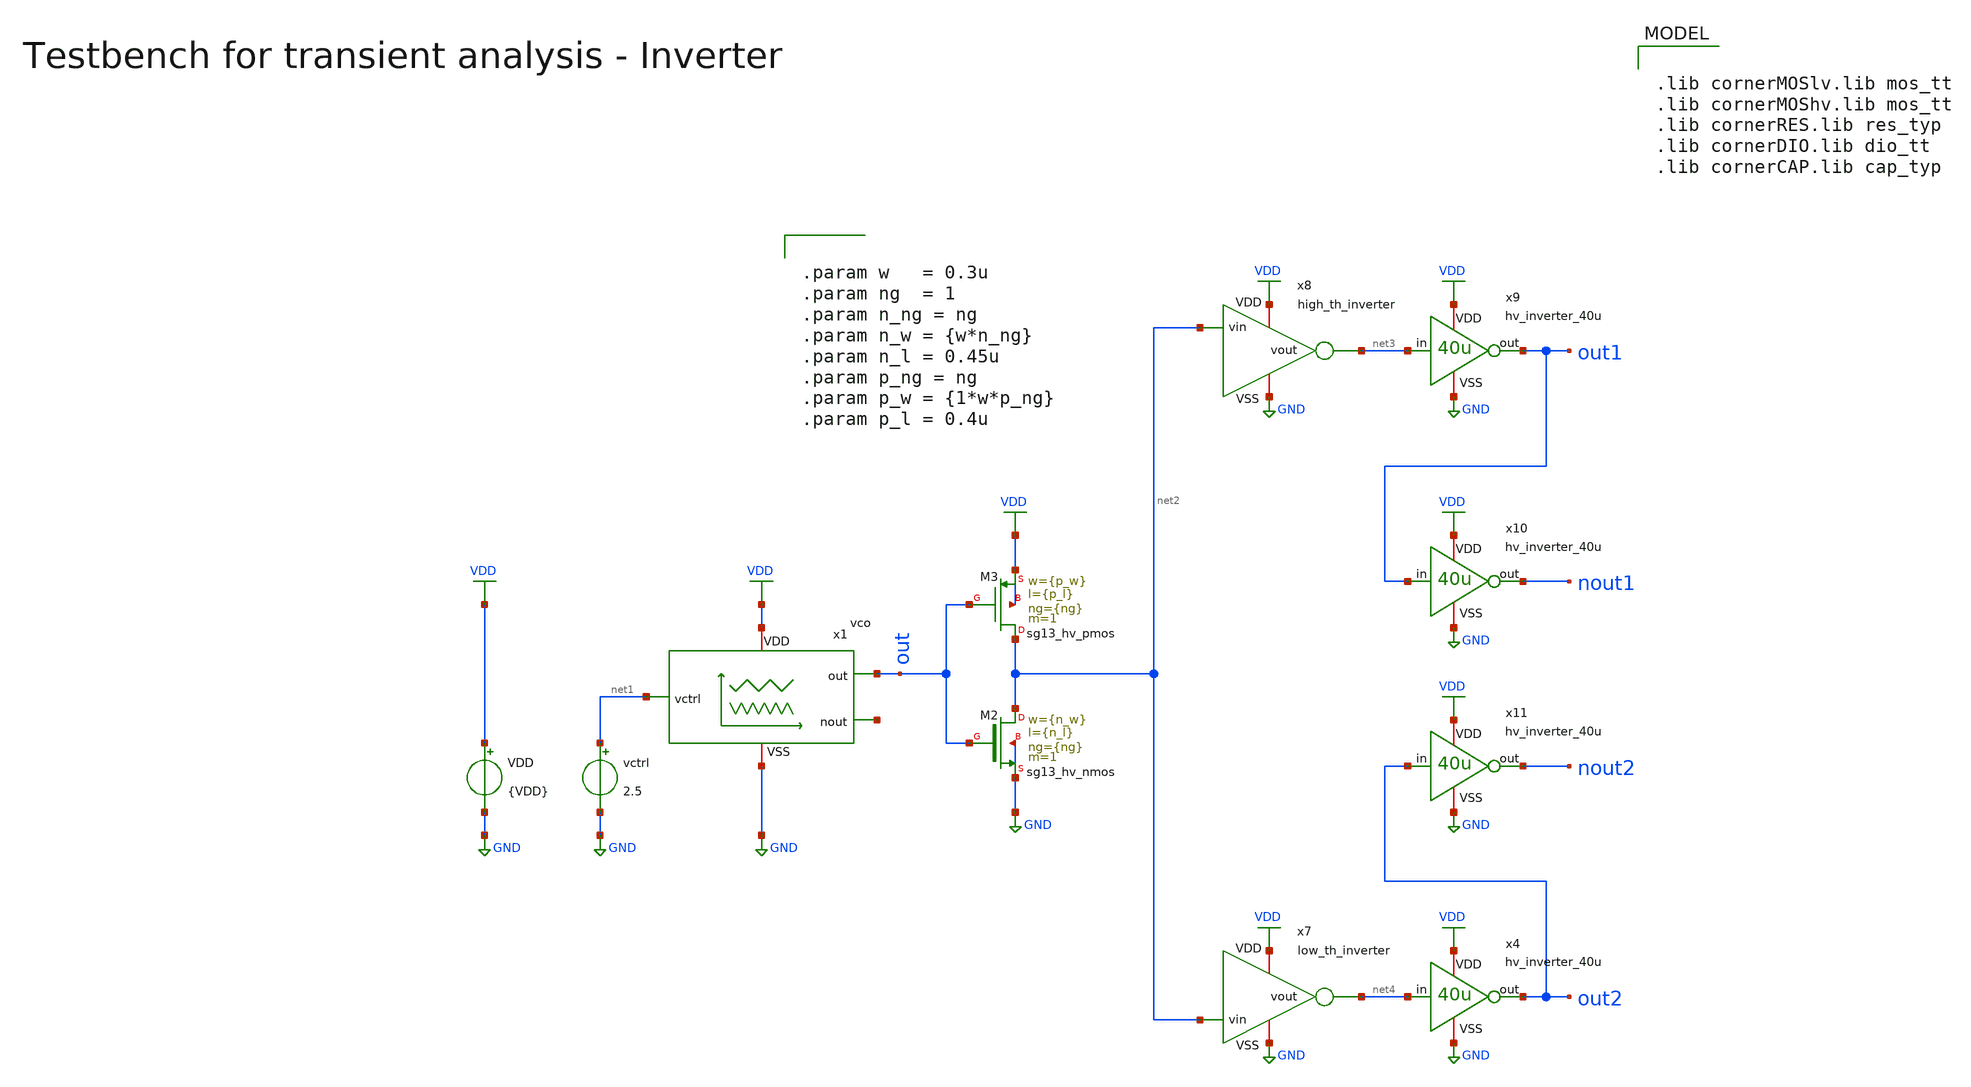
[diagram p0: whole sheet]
** sch_path: macros/heichips26_vcr/macros/switched_capacitor/testbenches/xschem/tb_vco_tran.sch
**.subckt tb_vco_tran
VDD VDD GND {VDD}
vctrl net1 GND 2.5
x1 VDD out net1 GND net5 vco
XM2 net2 out GND GND sg13_hv_nmos w={n_w} l={n_l} ng={ng} m=1 mm_ok=1
XM3 net2 out VDD VDD sg13_hv_pmos w={p_w} l={p_l} ng={ng} m=1 mm_ok=1
x4 VDD net4 out2 GND hv_inverter_40u
x7 VDD net2 net4 GND low_th_inverter
x8 VDD net2 net3 GND high_th_inverter
x9 VDD net3 out1 GND hv_inverter_40u
x10 VDD out1 nout1 GND hv_inverter_40u
x11 VDD out2 nout2 GND hv_inverter_40u
**** begin user architecture code


.param VDD=3.3
.csparam VDD=VDD
.param Vcm=VDD/2
.param temp=27
.param Cload=10p
.param Rload=1k

.param period = 2000n
.param ton    = {period*2}
.csparam tstop  = {2*period}
.csparam tstep  = {period/100}

.options savecurrents klu method=gear reltol=1e-4 abstol=1e-15 gmin=1e-15

.control

save all

* Operating Point Analysis
op
remzerovec
write @schname\.raw
set appendwrite

* Transient Analysis
tran {$&tstep} {$&tstop}
write @schname\.raw

* Plotting
*plot vc+12 thl+12 thh+12 s+8 r+4 vout
*plot vc thl thh vout
plot out
plot out1+4 out2+4 nout1 nout2

* Write Data
unset appendwrite
set wr_vecnames
set wr_singlescale
*wrdata ../plot_simulations/data/@schname\.txt v(vin1) v(vin2) v(vout)

*quit
.endc



.lib cornerMOSlv.lib mos_tt
.lib cornerMOShv.lib mos_tt
.lib cornerRES.lib res_typ
.lib cornerDIO.lib dio_tt
.lib cornerCAP.lib cap_typ



.param w   = 0.3u
.param ng  = 1
.param n_ng = ng
.param n_w = {w*n_ng}
.param n_l = 0.45u
.param p_ng = ng
.param p_w = {1*w*p_ng}
.param p_l = 0.4u


**** end user architecture code
**.ends

* expanding   symbol:  vco.sym # of pins=5
** sym_path: macros/heichips26_vcr/macros/switched_capacitor/schematic/xschem/vco.sym
** sch_path: macros/heichips26_vcr/macros/switched_capacitor/schematic/xschem/vco.sch
.subckt vco VDD out vctrl VSS nout
*.iopin VSS
*.iopin VDD
*.iopin nout
*.iopin out
*.iopin vctrl
**** begin user architecture code


.ic v(vc)=1.65


**** end user architecture code
XC1 vc VSS cap_cmomi w=30e-6 l=30e-6 mmin=1 mmax=4 feed=double subblock=0 m=1 mm_ok=1
XM4 vc out 5uA- VSS sg13_hv_nmos w=0.3u l=0.45u ng=1 m=1 mm_ok=1
x1 VDD s out nout r VSS hv_rs-ff
**** begin user architecture code


.param cm_n_w = 6u
.param cm_n_l = 5u
.param cm_p_w = 10u
.param cm_p_l = 2u

.param inv_ng = 1
.param inv_n_w = 2u
.param inv_n_l = 0.45u
.param inv_p_w = 6.5u
.param inv_p_l = 0.4u


**** end user architecture code
XM6 vc out 5uA+ VDD sg13_hv_pmos w=0.3u l=0.4u ng=1 m=1 mm_ok=1
x5 net2 vc vthl VDD 40uA- VSS comp_pmos
x4 VDD net3 VSS current_reference_40uA
XM7 s net1 VSS VSS sg13_hv_nmos w=inv_n_w l=inv_n_l ng=inv_ng m=1 mm_ok=1
XM8 s net1 VDD VDD sg13_hv_pmos w=inv_p_w l=inv_p_l ng=inv_ng m=1 mm_ok=1
XM9 r net2 VSS VSS sg13_hv_nmos w=inv_n_w l=inv_n_l ng=inv_ng m=1 mm_ok=1
XM10 r net2 VDD VDD sg13_hv_pmos w=inv_p_w l=inv_p_l ng=inv_ng m=1 mm_ok=1
x7 net1 vthh vc VDD 40uA+ VSS comp_nmos
XM11 net3 net3 VDD VDD sg13_hv_pmos w=cm_p_w l=cm_p_l ng=1 m=1 mm_ok=1
XM12 40uA+ net3 VDD VDD sg13_hv_pmos w=cm_p_w l=cm_p_l ng=1 m=1 mm_ok=1
XM13 net4 net3 VDD VDD sg13_hv_pmos w=cm_p_w l=cm_p_l ng=1 m=1 mm_ok=1
XM14 net4 net4 VSS VSS sg13_hv_nmos w=cm_n_w l=cm_n_l ng=1 m=1 mm_ok=1
XM15 40uA- net4 VSS VSS sg13_hv_nmos w=cm_n_w l=cm_n_l ng=1 m=1 mm_ok=1
x2 10uA- vthl VDD vctrl VSS vthh voltage_mirror_pmos
XM1 net5 net3 VDD VDD sg13_hv_pmos w=cm_p_w l=cm_p_l ng=1 m=1 mm_ok=1
XM2 net5 net5 VSS VSS sg13_hv_nmos w=4*cm_n_w l=cm_n_l ng=4 m=1 mm_ok=1
XM3 10uA- net5 VSS VSS sg13_hv_nmos w=cm_n_w l=cm_n_l ng=1 m=1 mm_ok=1
XM5 net6 net5 VSS VSS sg13_hv_nmos w=cm_n_w l=cm_n_l ng=1 m=1 mm_ok=1
XM25 net6 net6 VDD VDD sg13_hv_pmos w=2*cm_p_w l=cm_p_l ng=2 m=1 mm_ok=1
XM26 net7 net6 VDD VDD sg13_hv_pmos w=cm_p_w l=cm_p_l ng=1 m=1 mm_ok=1
XM27 5uA+ net6 VDD VDD sg13_hv_pmos w=cm_p_w l=cm_p_l ng=1 m=1 mm_ok=1
XM28 net7 net7 VSS VSS sg13_hv_nmos w=2*cm_n_w l=cm_n_l ng=2 m=1 mm_ok=1
XM29 5uA- net7 VSS VSS sg13_hv_nmos w=cm_n_w l=cm_n_l ng=1 m=1 mm_ok=1
.ends


* expanding   symbol:  hv_inverter_40u.sym # of pins=4
** sym_path: macros/heichips26_vcr/macros/switched_capacitor/schematic/xschem/hv_inverter_40u.sym
** sch_path: macros/heichips26_vcr/macros/switched_capacitor/schematic/xschem/hv_inverter_40u.sch
.subckt hv_inverter_40u VDD in out VSS
*.ipin in
*.iopin VDD
*.iopin VSS
*.opin out
XM2 out in VSS VSS sg13_hv_nmos w={n_w} l={n_l} ng={ng} m=1 mm_ok=1
XM3 out in VDD VDD sg13_hv_pmos w={p_w} l={p_l} ng={ng} m=1 mm_ok=1
**** begin user architecture code


.param w   = 10u
.param ng  = 4
.param n_ng = ng
.param n_w = {3u*n_ng}
.param n_l = 0.45u
.param p_ng = ng
.param p_w = {10u*p_ng}
.param p_l = 0.4u


**** end user architecture code
.ends


* expanding   symbol:  low_th_inverter.sym # of pins=4
** sym_path: macros/heichips26_vcr/macros/switched_capacitor/schematic/xschem/low_th_inverter.sym
** sch_path: macros/heichips26_vcr/macros/switched_capacitor/schematic/xschem/low_th_inverter.sch
.subckt low_th_inverter VDD vin vout VSS
*.ipin vin
*.iopin VDD
*.iopin VSS
*.opin vout
XM1 vout vin VSS VSS sg13_hv_nmos w={n_ng*n_w} l={n_l} ng={n_ng} m=1 mm_ok=1
XM2 vout vin VDD VDD sg13_hv_pmos w={p_ng*p_w} l={p_l} ng={n_ng} m=1 mm_ok=1
**** begin user architecture code


.param n_ng = 2
.param n_w = 1u
.param n_l = 0.45u
.param p_ng = 2
.param p_w = 1u
.param p_l = 0.4u


**** end user architecture code
.ends


* expanding   symbol:  high_th_inverter.sym # of pins=4
** sym_path: macros/heichips26_vcr/macros/switched_capacitor/schematic/xschem/high_th_inverter.sym
** sch_path: macros/heichips26_vcr/macros/switched_capacitor/schematic/xschem/high_th_inverter.sch
.subckt high_th_inverter VDD vin vout VSS
*.ipin vin
*.iopin VDD
*.iopin VSS
*.opin vout
XMdummy1 VSS VSS VSS VSS sg13_hv_nmos w=0.6u l=1.0u ng=2 m=1 mm_ok=1
XMdummy2 VDD VDD VDD VDD sg13_hv_pmos w=12.0u l=1.0u ng=2 m=1 mm_ok=1
XM1 vout vin VSS VSS sg13_hv_nmos w=6.0u l=1.0u ng=20 m=1 mm_ok=1
XM2 vout vin VDD VDD sg13_hv_pmos w=120.0u l=1.0u ng=20 m=1 mm_ok=1
.ends


* expanding   symbol:  hv_rs-ff.sym # of pins=6
** sym_path: macros/heichips26_vcr/macros/switched_capacitor/schematic/xschem/hv_rs-ff.sym
** sch_path: macros/heichips26_vcr/macros/switched_capacitor/schematic/xschem/hv_rs-ff.sch
.subckt hv_rs-ff VDD nS Q nQ nR VSS
*.ipin nS
*.iopin VDD
*.iopin VSS
*.opin Q
*.ipin nR
*.opin nQ
x4 VDD nS Q nQ VSS hv_nand
x5 VDD Q nQ nR VSS hv_nand
.ends


* expanding   symbol:  comp_pmos.sym # of pins=6
** sym_path: macros/heichips26_vcr/macros/switched_capacitor/schematic/xschem/comp_pmos.sym
** sch_path: macros/heichips26_vcr/macros/switched_capacitor/schematic/xschem/comp_pmos.sch
.subckt comp_pmos out - + VDD Ibias VSS
*.iopin VDD
*.iopin VSS
*.ipin Ibias
*.opin out
*.ipin +
*.ipin -
**** begin user architecture code


.param n_w = 1.2u
.param n_l = 1.5u
.param p_w = 2u
.param p_l = 0.4u
.param bcm = 1


**** end user architecture code
XM9 net1 Ibias VDD VDD sg13_hv_pmos w=bcm*p_w l=p_l ng=1 m=1 mm_ok=1
XM10 out Ibias VDD VDD sg13_hv_pmos w=bcm*p_w l=p_l ng=1 m=1 mm_ok=1
XM11 Ibias Ibias VDD VDD sg13_hv_pmos w=p_w l=p_l ng=1 m=1 mm_ok=1
XM12 net3 + net1 VDD sg13_hv_pmos w=p_w l=p_l ng=1 m=1 mm_ok=1
XM13 net2 - net1 VDD sg13_hv_pmos w=p_w l=p_l ng=1 m=1 mm_ok=1
XM14 net3 net2 VSS VSS sg13_hv_nmos w=n_w l=n_l ng=1 m=1 mm_ok=1
XM15 net2 net2 VSS VSS sg13_hv_nmos w=n_w l=n_l ng=1 m=1 mm_ok=1
XM16 out net3 VSS VSS sg13_hv_nmos w=n_w l=n_l ng=1 m=1 mm_ok=1
.ends


* expanding   symbol:  current_reference_40uA.sym # of pins=3
** sym_path: macros/heichips26_vcr/macros/switched_capacitor/schematic/xschem/current_reference_40uA.sym
** sch_path: macros/heichips26_vcr/macros/switched_capacitor/schematic/xschem/current_reference_40uA.sch
.subckt current_reference_40uA VDD iout VSS
*.iopin VSS
*.iopin VDD
*.iopin iout
XM8 net2 net2 VSS VSS sg13_hv_nmos w=n_w l=n_l ng=1 m=1 mm_ok=1
XM6 net2 net1 VDD VDD sg13_hv_pmos w=p_w l=p_l ng=1 m=1 mm_ok=1
XM1 net1 net1 VDD VDD sg13_hv_pmos w=p_w l=p_l ng=1 m=1 mm_ok=1
XM3 net1 net2 net3 VSS sg13_hv_nmos w=n_w l=n_l ng=1 m=1 mm_ok=1
XR2 net4 VSS VSS rppd w=2e-6 l=21.9e-6 m=1 b=0 mm_ok=1
XM2 net1 net2 net3 VSS sg13_hv_nmos w=n_w l=n_l ng=1 m=1 mm_ok=1
XM4 net1 net2 net3 VSS sg13_hv_nmos w=n_w l=n_l ng=1 m=1 mm_ok=1
XM5 net1 net2 net3 VSS sg13_hv_nmos w=n_w l=n_l ng=1 m=1 mm_ok=1
XM7 iout net2 VSS VSS sg13_hv_nmos w=n_w l=n_l ng=1 m=1 mm_ok=1
XR3 net3 net4 VSS rsil w=0.5e-6 l=365e-6 m=1 mm_ok=1
**** begin user architecture code


.param n_w = 6u
.param n_l = 5u
.param p_w = 10u
.param p_l = 2u


**** end user architecture code
.ends


* expanding   symbol:  comp_nmos.sym # of pins=6
** sym_path: macros/heichips26_vcr/macros/switched_capacitor/schematic/xschem/comp_nmos.sym
** sch_path: macros/heichips26_vcr/macros/switched_capacitor/schematic/xschem/comp_nmos.sch
.subckt comp_nmos out - + VDD Ibias VSS
*.iopin VDD
*.iopin VSS
*.ipin -
*.ipin +
*.ipin Ibias
*.opin out
XM8 net2 + net3 VSS sg13_hv_nmos w=n_w l=n_l ng=1 m=1 mm_ok=1
XM6 net1 net1 VDD VDD sg13_hv_pmos w=p_w l=p_l ng=1 m=1 mm_ok=1
XM1 net2 net1 VDD VDD sg13_hv_pmos w=p_w l=p_l ng=1 m=1 mm_ok=1
XM3 net1 - net3 VSS sg13_hv_nmos w=n_w l=n_l ng=1 m=1 mm_ok=1
**** begin user architecture code


.param n_w = 1.2u
.param n_l = 1.5u
.param p_w = 2u
.param p_l = 0.4u


**** end user architecture code
XM2 out net2 VDD VDD sg13_hv_pmos w=p_w l=p_l ng=1 m=1 mm_ok=1
XM4 net3 Ibias VSS VSS sg13_hv_nmos w=2*n_w l=n_l ng=1 m=1 mm_ok=1
XM5 out Ibias VSS VSS sg13_hv_nmos w=2*n_w l=n_l ng=1 m=1 mm_ok=1
XM7 Ibias Ibias VSS VSS sg13_hv_nmos w=n_w l=n_l ng=1 m=1 mm_ok=1
.ends


* expanding   symbol:  voltage_mirror_pmos.sym # of pins=6
** sym_path: macros/heichips26_vcr/macros/switched_capacitor/schematic/xschem/voltage_mirror_pmos.sym
** sch_path: macros/heichips26_vcr/macros/switched_capacitor/schematic/xschem/voltage_mirror_pmos.sch
.subckt voltage_mirror_pmos Ibias nout VDD in VSS out
*.iopin VDD
*.iopin VSS
*.ipin in
*.opin out
*.opin nout
*.ipin Ibias
**** begin user architecture code


.param n_w = 6u
.param n_l = 5u
.param p_w = 10u
.param p_l = 2u


**** end user architecture code
XR1 in Ibias VSS rhigh w=0.5e-6 l=34e-6 m=1 b=0 mm_ok=1
XM4 net1 Ibias VDD VDD sg13_hv_pmos w=p_w l=p_l ng=1 m=1 mm_ok=1
XM5 out net1 VSS VSS sg13_hv_nmos w=n_w l=n_l ng=1 m=1 mm_ok=1
XR2 VSS nout VSS rhigh w=0.5e-6 l=34e-6 m=1 b=0 mm_ok=1
XR3 out VDD VSS rhigh w=0.5e-6 l=34e-6 m=1 b=0 mm_ok=1
XM2 net1 net1 VSS VSS sg13_hv_nmos w=n_w l=n_l ng=1 m=1 mm_ok=1
XM3 nout Ibias VDD VDD sg13_hv_pmos w=p_w l=p_l ng=1 m=1 mm_ok=1
XM6 Ibias Ibias VDD VDD sg13_hv_pmos w=1.9*p_w l=p_l ng=1 m=1 mm_ok=1
.ends


* expanding   symbol:  hv_nand.sym # of pins=5
** sym_path: macros/heichips26_vcr/macros/switched_capacitor/schematic/xschem/hv_nand.sym
** sch_path: macros/heichips26_vcr/macros/switched_capacitor/schematic/xschem/hv_nand.sch
.subckt hv_nand VDD in1 out in2 VSS
*.ipin in1
*.iopin VDD
*.iopin VSS
*.opin out
*.ipin in2
**** begin user architecture code


.param w   = 10u
.param ng  = 4
.param n_ng = ng
.param n_w = {3u*n_ng}
.param n_l = 0.45u
.param p_ng = ng
.param p_w = {10u*p_ng}
.param p_l = 0.4u


**** end user architecture code
XM2 out in1 net1 VSS sg13_hv_nmos w={n_w} l={n_l} ng={ng} m=1 mm_ok=1
XM3 out in2 VDD VDD sg13_hv_pmos w={p_w} l={p_l} ng={ng} m=1 mm_ok=1
XM1 net1 in2 VSS VSS sg13_hv_nmos w={n_w} l={n_l} ng={ng} m=1 mm_ok=1
XM4 out in1 VDD VDD sg13_hv_pmos w={p_w} l={p_l} ng={ng} m=1 mm_ok=1
.ends

.GLOBAL VDD
.GLOBAL GND
.end
